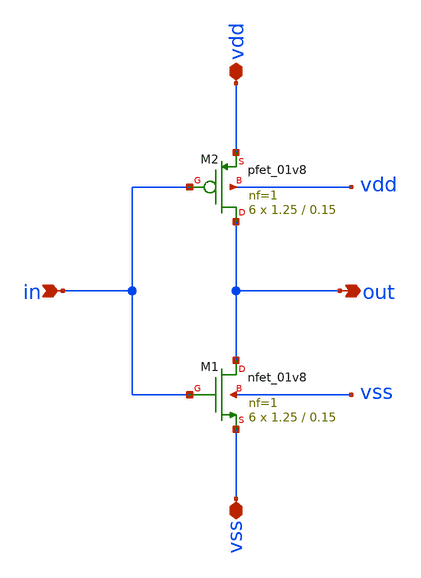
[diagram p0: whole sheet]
** sch_path: xschem/inverter_cp_x2.sch
**.subckt inverter_cp_x2 vss in out vdd
*.iopin vss
*.ipin in
*.opin out
*.iopin vdd
XM2 out in vdd vdd sky130_fd_pr__pfet_01v8 L=0.15 W=1.25 nf=1 ad='int((nf+1)/2) * W/nf * 0.29' as='int((nf+2)/2) * W/nf * 0.29'
+ pd='2*int((nf+1)/2) * (W/nf + 0.29)' ps='2*int((nf+2)/2) * (W/nf + 0.29)' nrd='0.29 / W' nrs='0.29 / W'
+ sa=0 sb=0 sd=0 mult=6 m=6
XM1 out in vss vss sky130_fd_pr__nfet_01v8 L=0.15 W=1.25 nf=1 ad='int((nf+1)/2) * W/nf * 0.29' as='int((nf+2)/2) * W/nf * 0.29'
+ pd='2*int((nf+1)/2) * (W/nf + 0.29)' ps='2*int((nf+2)/2) * (W/nf + 0.29)' nrd='0.29 / W' nrs='0.29 / W'
+ sa=0 sb=0 sd=0 mult=6 m=6
**.ends
.end
